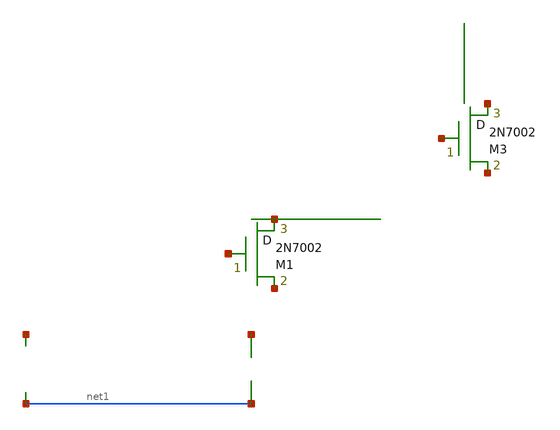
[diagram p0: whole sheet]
** sch_path: tests/fixtures/hierarchy/top.sch
**.subckt top
R1 net2 net1 10k m=1
X1 amp
C1 net3 net1 100n m=1
**.ends

* expanding   symbol:  sub/amp.sch # of pins=0
** sym_path: tests/fixtures/hierarchy/sub/amp.sch
** sch_path: tests/fixtures/hierarchy/sub/amp.sch
.subckt amp
M1 net1 net2 net3 nfet m=1
X2 bias
.ends


* expanding   symbol:  sub/bias.sch # of pins=0
** sym_path: tests/fixtures/hierarchy/sub/bias.sch
** sch_path: tests/fixtures/hierarchy/sub/bias.sch
.subckt bias
M3 net2 net3 net4 nfet m=1
.ends

.end
